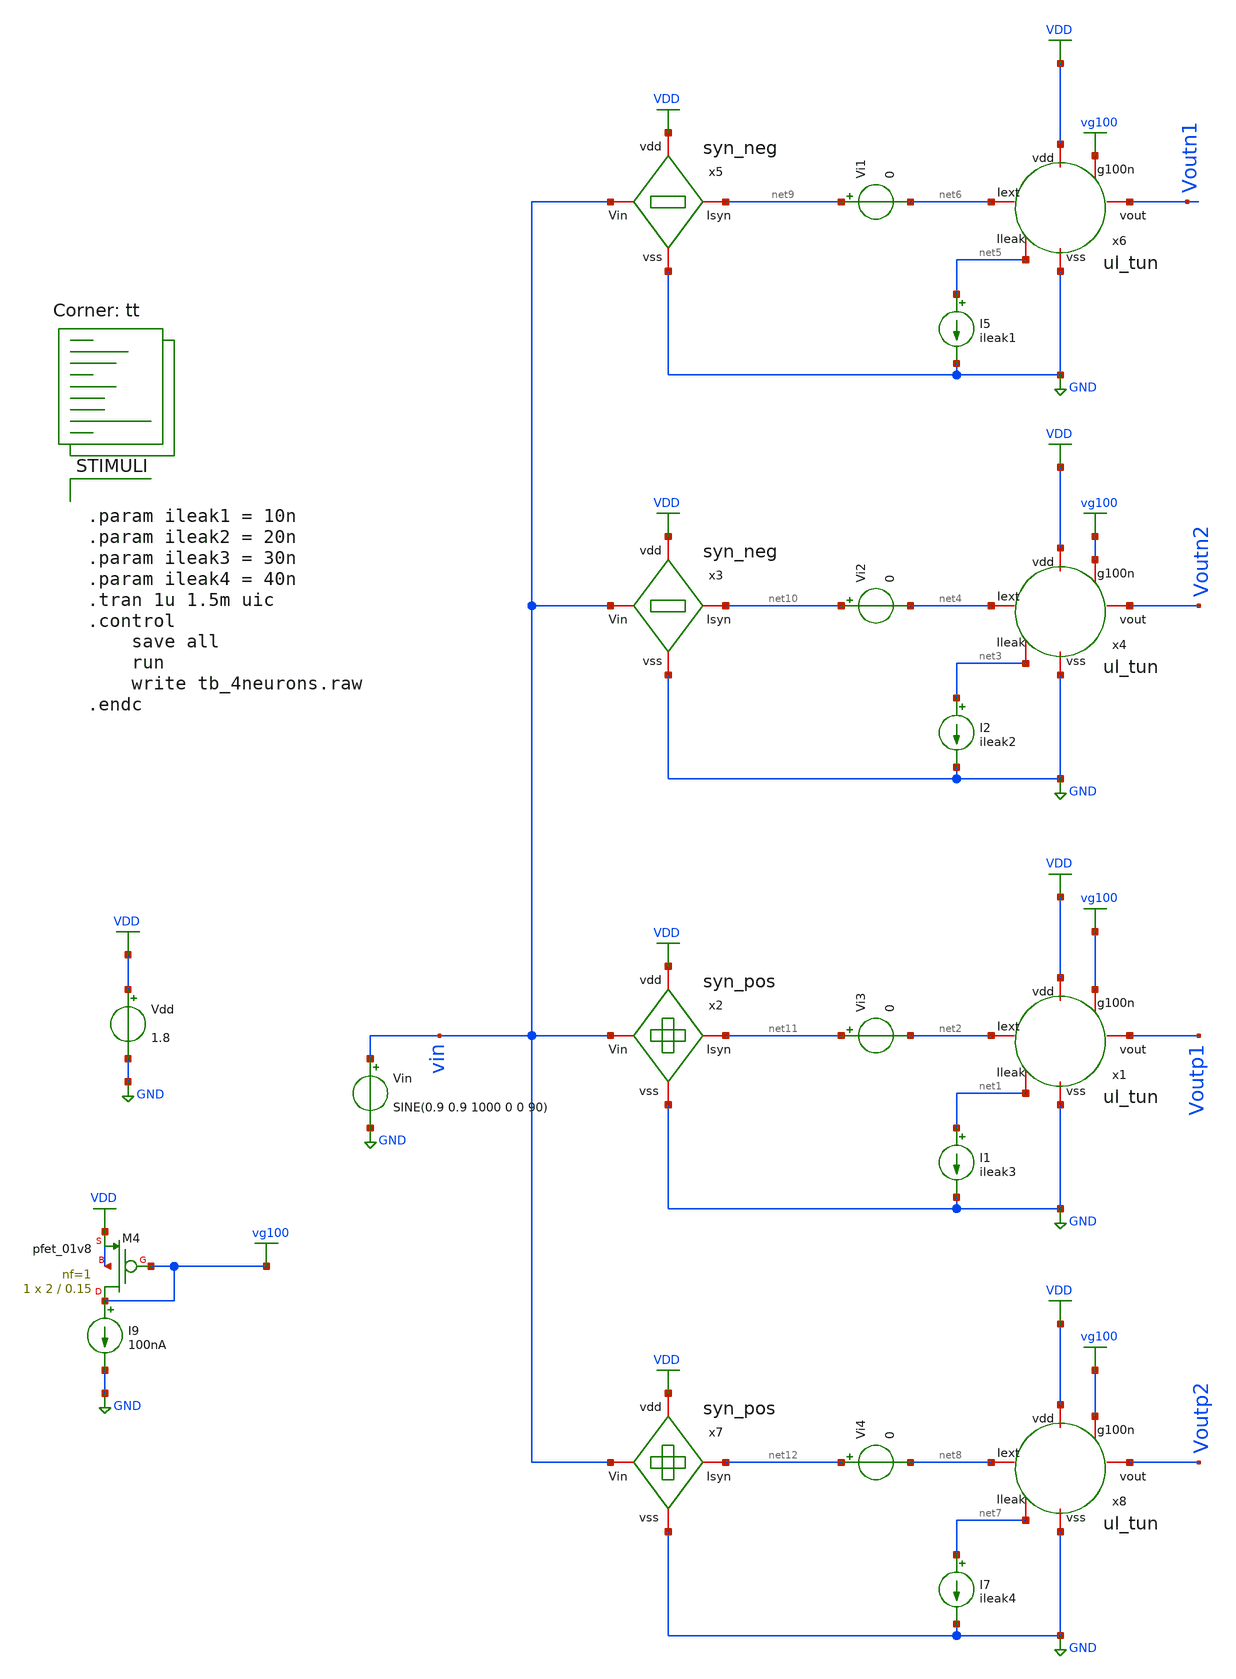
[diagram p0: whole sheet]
** sch_path: tb_4neurons.sch
**.subckt tb_4neurons
I1 net1 GND ileak3
Vdd VDD GND 1.8
Vin vin GND SINE(0.9 0.9 1000 0 0 90)
x2 VDD vin net11 GND syn_pos
x1 net2 VDD vg100 Voutp1 net1 GND ul_tun
I2 net3 GND ileak2
x3 VDD vin net10 GND syn_neg
x4 net4 VDD vg100 Voutn2 net3 GND ul_tun
I5 net5 GND ileak1
x5 VDD vin net9 GND syn_neg
x6 net6 VDD vg100 Voutn1 net5 GND ul_tun
I7 net7 GND ileak4
x7 VDD vin net12 GND syn_pos
x8 net8 VDD vg100 Voutp2 net7 GND ul_tun
I9 vg100 GND 100nA
XM4 vg100 vg100 VDD VDD sky130_fd_pr__pfet_01v8 L=0.15 W=2 nf=1 ad='int((nf+1)/2) * W/nf * 0.29' as='int((nf+2)/2) * W/nf * 0.29'
+ pd='2*int((nf+1)/2) * (W/nf + 0.29)' ps='2*int((nf+2)/2) * (W/nf + 0.29)' nrd='0.29 / W' nrs='0.29 / W'
+ sa=0 sb=0 sd=0 mult=1 m=1
Vi1 net9 net6 0
Vi2 net10 net4 0
Vi3 net11 net2 0
Vi4 net12 net8 0
**** begin user architecture code
.lib $::SKYWATER_MODELS/sky130.lib.spice tt

** opencircuitdesign pdks install
*.inc $::SKYWATER_MODELS/rram_v0.spice
.inc /home/alex/Desktop/EDA/SNN_IPN/memristor_models/wellposed/wllpsd.spice


**** end user architecture code
**.ends

* expanding   symbol:  /home/alex/Desktop/EDA/SNN_IPN/Neuron/ultralif/syn_pos.sym # of pins=4
** sym_path: Neuron/ultralif/syn_pos.sym
** sch_path: Neuron/ultralif/syn_pos.sch
.subckt syn_pos vdd Vin Isyn vss
*.iopin Vin
*.iopin vdd
*.iopin vss
*.iopin Isyn
XM9 Isyn vx vdd vdd sky130_fd_pr__pfet_01v8 L=1 W=0.5 nf=1 ad='int((nf+1)/2) * W/nf * 0.29' as='int((nf+2)/2) * W/nf * 0.29'
+ pd='2*int((nf+1)/2) * (W/nf + 0.29)' ps='2*int((nf+2)/2) * (W/nf + 0.29)' nrd='0.29 / W' nrs='0.29 / W'
+ sa=0 sb=0 sd=0 mult=1 m=1
XM10 vx vx vdd vdd sky130_fd_pr__pfet_01v8 L=0.15 W=0.5 nf=1 ad='int((nf+1)/2) * W/nf * 0.29' as='int((nf+2)/2) * W/nf * 0.29'
+ pd='2*int((nf+1)/2) * (W/nf + 0.29)' ps='2*int((nf+2)/2) * (W/nf + 0.29)' nrd='0.29 / W' nrs='0.29 / W'
+ sa=0 sb=0 sd=0 mult=5 m=5
XM12 vx Vin vss vss sky130_fd_pr__nfet_01v8 L=1 W=0.4 nf=1 ad='int((1 + 1)/2) * 0.4 / 1 * 0.29' as='int((1 + 2)/2) * 0.4 / 1 * 0.29'
+ pd='2*int((1 + 1)/2) * (0.4 / 1 + 0.29)' ps='2*int((1 + 2)/2) * (0.4 / 1 + 0.29)' nrd='0.29 / 0.4 ' nrs='0.29 / 0.4 '
+ sa=0 sb=0 sd=0 mult=1 m=1
.ends


* expanding   symbol:  /home/alex/Desktop/EDA/SNN_IPN/Neuron/ultralif/ul_tun.sym # of pins=6
** sym_path: Neuron/ultralif/ul_tun.sym
** sch_path: Neuron/ultralif/ul_tun.sch
.subckt ul_tun Iext vdd g100n vout Ileak vss
*.iopin Iext
*.iopin vout
*.iopin vss
*.iopin Ileak
*.iopin vdd
*.iopin g100n
XM1 Ileak Ileak net1 vdd sky130_fd_pr__pfet_01v8 L=10 W=1 nf=1 ad='int((nf+1)/2) * W/nf * 0.29' as='int((nf+2)/2) * W/nf * 0.29'
+ pd='2*int((nf+1)/2) * (W/nf + 0.29)' ps='2*int((nf+2)/2) * (W/nf + 0.29)' nrd='0.29 / W' nrs='0.29 / W'
+ sa=0 sb=0 sd=0 mult=1 m=1
XM2 Ileak net2 net1 vdd sky130_fd_pr__pfet_01v8 L=0.15 W=1.5 nf=1 ad='int((nf+1)/2) * W/nf * 0.29' as='int((nf+2)/2) * W/nf * 0.29'
+ pd='2*int((nf+1)/2) * (W/nf + 0.29)' ps='2*int((nf+2)/2) * (W/nf + 0.29)' nrd='0.29 / W' nrs='0.29 / W'
+ sa=0 sb=0 sd=0 mult=1 m=1
XM3 net2 net2 net1 vdd sky130_fd_pr__pfet_01v8 L=0.15 W=15 nf=1 ad='int((nf+1)/2) * W/nf * 0.29' as='int((nf+2)/2) * W/nf * 0.29'
+ pd='2*int((nf+1)/2) * (W/nf + 0.29)' ps='2*int((nf+2)/2) * (W/nf + 0.29)' nrd='0.29 / W' nrs='0.29 / W'
+ sa=0 sb=0 sd=0 mult=1 m=1
XM4 net2 Ileak vss vss sky130_fd_pr__nfet_01v8 L=4 W=1 nf=1 ad='int((1 + 1)/2) * 1 / 1 * 0.29' as='int((1 + 2)/2) * 1 / 1 * 0.29'
+ pd='2*int((1 + 1)/2) * (1 / 1 + 0.29)' ps='2*int((1 + 2)/2) * (1 / 1 + 0.29)' nrd='0.29 / 1 ' nrs='0.29 / 1 '
+ sa=0 sb=0 sd=0 mult=1 m=1
C1 net1 vss 1p m=1
XM5 vout_n Ileak vss vss sky130_fd_pr__nfet_01v8 L=0.15 W=1 nf=1 ad='int((1 + 1)/2) * 1 / 1 * 0.29' as='int((1 + 2)/2) * 1 / 1 * 0.29'
+ pd='2*int((1 + 1)/2) * (1 / 1 + 0.29)' ps='2*int((1 + 2)/2) * (1 / 1 + 0.29)' nrd='0.29 / 1 ' nrs='0.29 / 1 '
+ sa=0 sb=0 sd=0 mult=1 m=1
XM6 vout_n g100n vdd vdd sky130_fd_pr__pfet_01v8 L=0.15 W=2 nf=1 ad='int((nf+1)/2) * W/nf * 0.29' as='int((nf+2)/2) * W/nf * 0.29'
+ pd='2*int((nf+1)/2) * (W/nf + 0.29)' ps='2*int((nf+2)/2) * (W/nf + 0.29)' nrd='0.29 / W' nrs='0.29 / W'
+ sa=0 sb=0 sd=0 mult=1 m=1
XM7 vout vout_n vss vss sky130_fd_pr__nfet_01v8 L=0.15 W=1 nf=1 ad='int((1 + 1)/2) * 1 / 1 * 0.29' as='int((1 + 2)/2) * 1 / 1 * 0.29'
+ pd='2*int((1 + 1)/2) * (1 / 1 + 0.29)' ps='2*int((1 + 2)/2) * (1 / 1 + 0.29)' nrd='0.29 / 1 ' nrs='0.29 / 1 '
+ sa=0 sb=0 sd=0 mult=1 m=1
XM8 vout vout_n vdd vdd sky130_fd_pr__pfet_01v8 L=0.15 W=2 nf=1 ad='int((nf+1)/2) * W/nf * 0.29' as='int((nf+2)/2) * W/nf * 0.29'
+ pd='2*int((nf+1)/2) * (W/nf + 0.29)' ps='2*int((nf+2)/2) * (W/nf + 0.29)' nrd='0.29 / W' nrs='0.29 / W'
+ sa=0 sb=0 sd=0 mult=1 m=1
vext Iext net1 0
**** begin user architecture code


.save i(vext)


**** end user architecture code
.ends


* expanding   symbol:  /home/alex/Desktop/EDA/SNN_IPN/Neuron/ultralif/syn_neg.sym # of pins=4
** sym_path: Neuron/ultralif/syn_neg.sym
** sch_path: Neuron/ultralif/syn_neg.sch
.subckt syn_neg vdd Vin Isyn vss
*.iopin Vin
*.iopin Isyn
*.iopin vdd
*.iopin vss
XM10 Isyn Vin vx vdd sky130_fd_pr__pfet_01v8 L=35 W=0.5 nf=1 ad='int((nf+1)/2) * W/nf * 0.29' as='int((nf+2)/2) * W/nf * 0.29'
+ pd='2*int((nf+1)/2) * (W/nf + 0.29)' ps='2*int((nf+2)/2) * (W/nf + 0.29)' nrd='0.29 / W' nrs='0.29 / W'
+ sa=0 sb=0 sd=0 mult=1 m=1
XM1 vx Vin vdd vdd sky130_fd_pr__pfet_01v8 L=35 W=0.5 nf=1 ad='int((nf+1)/2) * W/nf * 0.29' as='int((nf+2)/2) * W/nf * 0.29'
+ pd='2*int((nf+1)/2) * (W/nf + 0.29)' ps='2*int((nf+2)/2) * (W/nf + 0.29)' nrd='0.29 / W' nrs='0.29 / W'
+ sa=0 sb=0 sd=0 mult=1 m=1
XM2 Isyn net1 vdd vdd sky130_fd_pr__pfet_01v8 L=1 W=0.5 nf=1 ad='int((nf+1)/2) * W/nf * 0.29' as='int((nf+2)/2) * W/nf * 0.29'
+ pd='2*int((nf+1)/2) * (W/nf + 0.29)' ps='2*int((nf+2)/2) * (W/nf + 0.29)' nrd='0.29 / W' nrs='0.29 / W'
+ sa=0 sb=0 sd=0 mult=1 m=1
XR1 net1 vdd sky130_fd_pr__res_generic_po W=1.15 L=1 m=1
XR2 vss net1 sky130_fd_pr__res_generic_po W=1 L=1 m=1
.ends

.GLOBAL GND
.GLOBAL VDD
.GLOBAL vg100
**** begin user architecture code


.param ileak1 = 10n
.param ileak2 = 20n
.param ileak3 = 30n
.param ileak4 = 40n
.tran 1u 1.5m uic
.control
	save all
	run
	write tb_4neurons.raw
.endc


**** end user architecture code
.end
